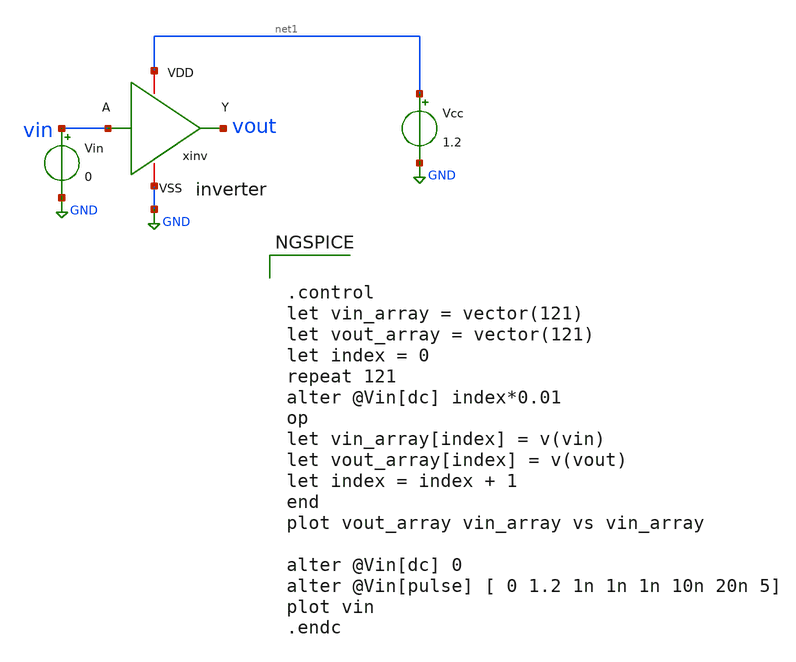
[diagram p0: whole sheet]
** sch_path: xschem/inverter_tb.sch
**.subckt inverter_tb
xinv net1 vin vout GND inverter
Vin vin GND 0
Vcc net1 GND 1.2
**** begin user architecture code


.control
let vin_array = vector(121)
let vout_array = vector(121)
let index = 0
repeat 121
alter @Vin[dc] index*0.01
op
let vin_array[index] = v(vin)
let vout_array[index] = v(vout)
let index = index + 1
end
plot vout_array vin_array vs vin_array

alter @Vin[dc] 0
alter @Vin[pulse] [ 0 1.2 1n 1n 1n 10n 20n 5]
plot vin
.endc


**** end user architecture code
**.ends

* expanding   symbol:  inverter.sym # of pins=4
** sym_path: xschem/inverter.sym
** sch_path: xschem/inverter.sch
.subckt inverter VDD A Y VSS
*.ipin A
*.opin Y
*.iopin VDD
*.iopin VSS
XM1 Y A VSS VSS sg13_lv_nmos w=150n l=130n ng=1 m=1 rfmode=1 mm_ok=1
XM2 Y A VDD VDD sg13_lv_pmos w=150n l=130n ng=1 m=1 rfmode=1 mm_ok=1
**** begin user architecture code

.lib cornerMOSlv.lib mos_tt

**** end user architecture code
.ends

.GLOBAL GND
.end
